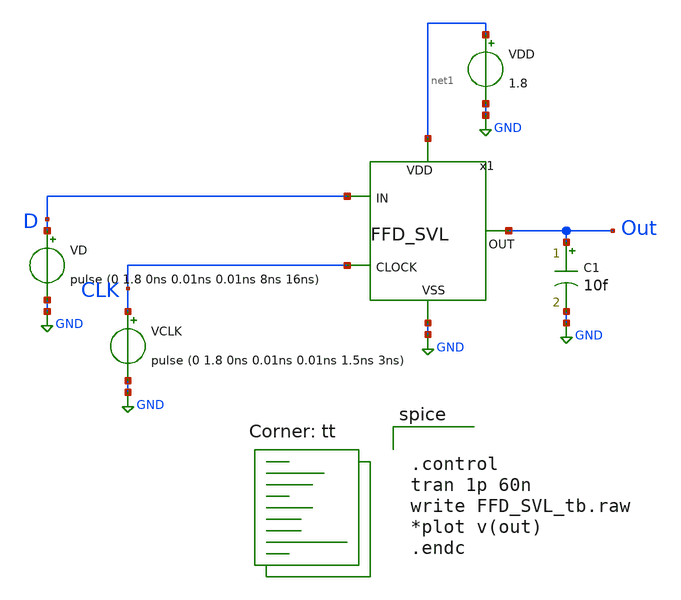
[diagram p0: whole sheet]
** sch_path: FFD_SVL_tb.sch
**.subckt FFD_SVL_tb
x1 net1 CLK D Out GND FFD_SVL
VD D GND pulse (0 1.8 0ns 0.01ns 0.01ns 8ns 16ns)
VCLK CLK GND pulse (0 1.8 0ns 0.01ns 0.01ns 1.5ns 3ns)
VDD net1 GND 1.8
C1 Out GND 10f m=1
**** begin user architecture code
.lib $::SKYWATER_MODELS/sky130.lib.spice tt


.control
tran 1p 60n
write FFD_SVL_tb.raw
*plot v(out)
.endc


**** end user architecture code
**.ends

* expanding   symbol:  project/FFD_SVL.sym # of pins=5
** sym_path: FFD_SVL.sym
** sch_path: FFD_SVL.sch
.subckt FFD_SVL VDD CLOCK IN OUT VSS
*.ipin VDD
*.ipin VSS
*.opin OUT
*.ipin IN
*.ipin CLOCK
XM1 net1 CLKB VDD VDD sky130_fd_pr__pfet_01v8 L=0.15 W=1 nf=1 ad='int((nf+1)/2) * W/nf * 0.29' as='int((nf+2)/2) * W/nf * 0.29'
+ pd='2*int((nf+1)/2) * (W/nf + 0.29)' ps='2*int((nf+2)/2) * (W/nf + 0.29)' nrd='0.29 / W' nrs='0.29 / W'
+ sa=0 sb=0 sd=0 mult=1 m=1
XM2 VDD VDD net1 VDD sky130_fd_pr__nfet_01v8 L=0.15 W=1 nf=1 ad='int((nf+1)/2) * W/nf * 0.29' as='int((nf+2)/2) * W/nf * 0.29'
+ pd='2*int((nf+1)/2) * (W/nf + 0.29)' ps='2*int((nf+2)/2) * (W/nf + 0.29)' nrd='0.29 / W' nrs='0.29 / W'
+ sa=0 sb=0 sd=0 mult=1 m=1
XM3 VSS VSS net4 VDD sky130_fd_pr__pfet_01v8 L=0.15 W=1 nf=1 ad='int((nf+1)/2) * W/nf * 0.29' as='int((nf+2)/2) * W/nf * 0.29'
+ pd='2*int((nf+1)/2) * (W/nf + 0.29)' ps='2*int((nf+2)/2) * (W/nf + 0.29)' nrd='0.29 / W' nrs='0.29 / W'
+ sa=0 sb=0 sd=0 mult=1 m=1
XM4 net4 CLK VSS VSS sky130_fd_pr__nfet_01v8 L=0.15 W=1 nf=1 ad='int((nf+1)/2) * W/nf * 0.29' as='int((nf+2)/2) * W/nf * 0.29'
+ pd='2*int((nf+1)/2) * (W/nf + 0.29)' ps='2*int((nf+2)/2) * (W/nf + 0.29)' nrd='0.29 / W' nrs='0.29 / W'
+ sa=0 sb=0 sd=0 mult=1 m=1
XM5 net2 IN net1 VDD sky130_fd_pr__pfet_01v8 L=0.15 W=1 nf=1 ad='int((nf+1)/2) * W/nf * 0.29' as='int((nf+2)/2) * W/nf * 0.29'
+ pd='2*int((nf+1)/2) * (W/nf + 0.29)' ps='2*int((nf+2)/2) * (W/nf + 0.29)' nrd='0.29 / W' nrs='0.29 / W'
+ sa=0 sb=0 sd=0 mult=1 m=1
XM6 OUT net2 net1 VDD sky130_fd_pr__pfet_01v8 L=0.15 W=1 nf=1 ad='int((nf+1)/2) * W/nf * 0.29' as='int((nf+2)/2) * W/nf * 0.29'
+ pd='2*int((nf+1)/2) * (W/nf + 0.29)' ps='2*int((nf+2)/2) * (W/nf + 0.29)' nrd='0.29 / W' nrs='0.29 / W'
+ sa=0 sb=0 sd=0 mult=1 m=1
XM7 net2 CLK net3 VSS sky130_fd_pr__nfet_01v8 L=0.15 W=1 nf=1 ad='int((nf+1)/2) * W/nf * 0.29' as='int((nf+2)/2) * W/nf * 0.29'
+ pd='2*int((nf+1)/2) * (W/nf + 0.29)' ps='2*int((nf+2)/2) * (W/nf + 0.29)' nrd='0.29 / W' nrs='0.29 / W'
+ sa=0 sb=0 sd=0 mult=1 m=1
XM8 net3 IN net4 VSS sky130_fd_pr__nfet_01v8 L=0.15 W=1 nf=1 ad='int((nf+1)/2) * W/nf * 0.29' as='int((nf+2)/2) * W/nf * 0.29'
+ pd='2*int((nf+1)/2) * (W/nf + 0.29)' ps='2*int((nf+2)/2) * (W/nf + 0.29)' nrd='0.29 / W' nrs='0.29 / W'
+ sa=0 sb=0 sd=0 mult=1 m=1
XM9 OUT net3 net4 VSS sky130_fd_pr__nfet_01v8 L=0.15 W=1 nf=1 ad='int((nf+1)/2) * W/nf * 0.29' as='int((nf+2)/2) * W/nf * 0.29'
+ pd='2*int((nf+1)/2) * (W/nf + 0.29)' ps='2*int((nf+2)/2) * (W/nf + 0.29)' nrd='0.29 / W' nrs='0.29 / W'
+ sa=0 sb=0 sd=0 mult=1 m=1
x7 VDD CLOCK CLKB VSS Inverter
x8 VDD CLKB CLK VSS Inverter
.ends


* expanding   symbol:  project/Inverter.sym # of pins=4
** sym_path: Inverter.sym
** sch_path: Inverter.sch
.subckt Inverter VDD IN OUT VSS
*.ipin IN
*.ipin VSS
*.ipin VDD
*.opin OUT
XM1 OUT IN VSS VSS sky130_fd_pr__nfet_01v8 L=0.3 W=1 nf=1 ad='int((nf+1)/2) * W/nf * 0.29' as='int((nf+2)/2) * W/nf * 0.29'
+ pd='2*int((nf+1)/2) * (W/nf + 0.29)' ps='2*int((nf+2)/2) * (W/nf + 0.29)' nrd='0.29 / W' nrs='0.29 / W'
+ sa=0 sb=0 sd=0 mult=1 m=1
XM2 OUT IN VDD VDD sky130_fd_pr__pfet_01v8 L=0.3 W=2 nf=1 ad='int((nf+1)/2) * W/nf * 0.29' as='int((nf+2)/2) * W/nf * 0.29'
+ pd='2*int((nf+1)/2) * (W/nf + 0.29)' ps='2*int((nf+2)/2) * (W/nf + 0.29)' nrd='0.29 / W' nrs='0.29 / W'
+ sa=0 sb=0 sd=0 mult=1 m=1
.ends

.GLOBAL GND
.end
